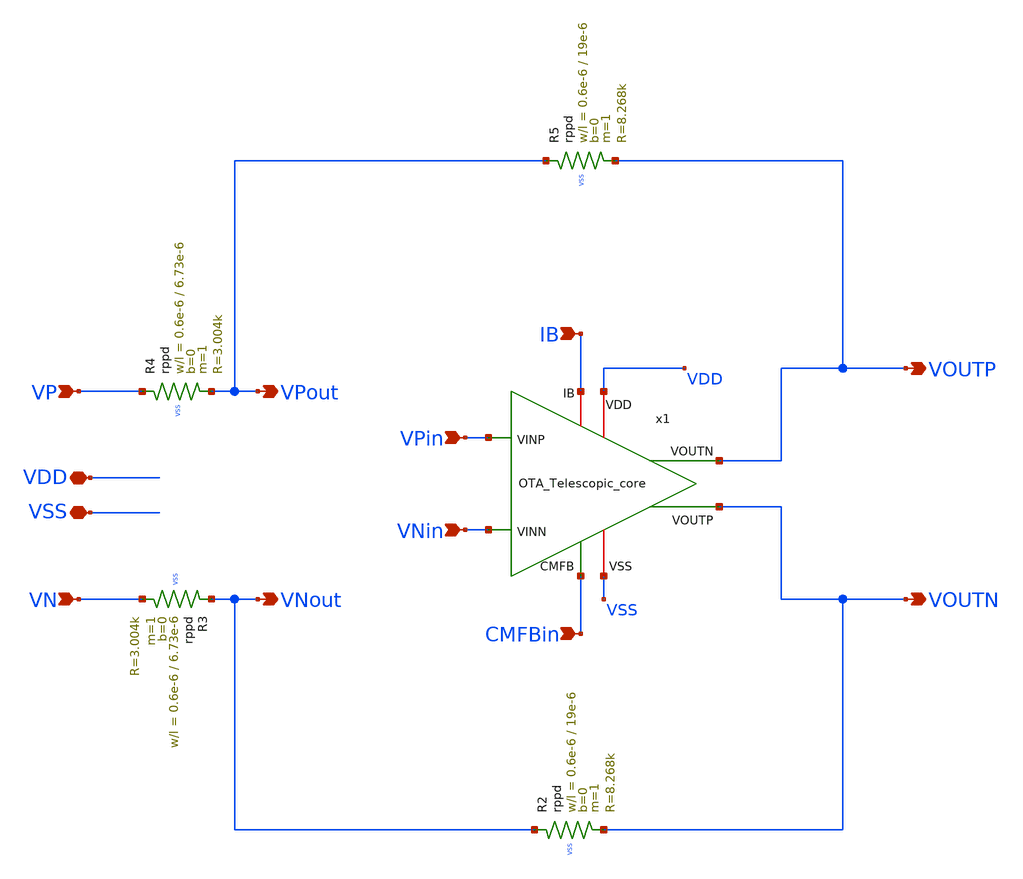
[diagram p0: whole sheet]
** sch_path: OTA_Telescopic_backup/OTA_Telescopic_NO_FLATTEN/Schematics_and_Symbols/OTA_Telescopic_FB.sch
**.subckt OTA_Telescopic_FB VP VN VOUTP VOUTN VPin VNin VPout VNout VDD VSS CMFBin IB
*.ipin VP
*.ipin VN
*.opin VOUTP
*.opin VOUTN
*.ipin VPin
*.ipin VNin
*.opin VPout
*.opin VNout
*.iopin VDD
*.iopin VSS
*.ipin CMFBin
*.ipin IB
x1 VDD CMFBin VOUTN VOUTP VPin VNin VSS IB OTA_Telescopic_core
XR3 VNout VN VSS rppd w=0.6e-6 l=6.73e-6 m=1 b=0 mm_ok=1
XR4 VP VPout VSS rppd w=0.6e-6 l=6.73e-6 m=1 b=0 mm_ok=1
XR5 VPout VOUTP VSS rppd w=0.6e-6 l=19e-6 m=1 b=0 mm_ok=1
XR2 VNout VOUTN VSS rppd w=0.6e-6 l=19e-6 m=1 b=0 mm_ok=1
**.ends

* expanding   symbol:  OTA_Telescopic_core.sym # of pins=8
** sym_path: OTA_Telescopic_core.sym
** sch_path: OTA_Telescopic_core.sch
.subckt OTA_Telescopic_core VDD CMFB VOUTP VOUTN VINP VINN VSS IB
*.iopin VDD
*.iopin VSS
*.ipin VINP
*.ipin VINN
*.opin VOUTN
*.opin VOUTP
*.ipin CMFB
*.iopin IB
V2 VB2 VSS 1.5
V3 VB3 VSS 0.7
V4 VB4 VSS 0.49409
V1 VB5 VSS 1.15
* noconn VB2
* noconn VB3
* noconn VB4
* noconn VB5
V5 VB VSS 0.90204
* noconn VB
XM15 VB55 VB55 VDD VDD sg13_lv_pmos w=1.4u l=0.35u ng=1 m=8 mm_ok=1
XM17 VB33 VB33 VDD VDD sg13_lv_pmos w=2.05u l=0.35u ng=1 m=1 mm_ok=1
XM18 VB22 VB33 VDD VDD sg13_lv_pmos w=2.05u l=0.35u ng=1 m=1 mm_ok=1
XM9 VOUTP Vo1 VDD VDD sg13_lv_pmos w=1.37u l=0.35u ng=1 m=250 mm_ok=1
XM7 Vx1 VB55 VDD VDD sg13_lv_pmos w=7u l=0.7u ng=1 m=30 mm_ok=1
XM5 Vo1 VB33 Vx1 VDD sg13_lv_pmos w=4.05u l=0.5u ng=1 m=30 mm_ok=1
XM8 Vx2 VB55 VDD VDD sg13_lv_pmos w=7u l=0.7u ng=1 m=30 mm_ok=1
XM6 Vo2 VB33 Vx2 VDD sg13_lv_pmos w=4.05u l=0.5u ng=1 m=30 mm_ok=1
XM10 VOUTN Vo2 VDD VDD sg13_lv_pmos w=1.37u l=0.35u ng=1 m=250 mm_ok=1
XM13 IB IB VSS VSS sg13_lv_nmos w=4.8u l=1.06u ng=1 m=1 mm_ok=1
XM14 VB55 IB VSS VSS sg13_lv_nmos w=4.8u l=1.06u ng=1 m=1 mm_ok=1
XM16 VB33 IB VSS VSS sg13_lv_nmos w=4.8u l=1.06u ng=1 m=1 mm_ok=1
XM19 VB22 VB22 VSS VSS sg13_lv_nmos w=0.5u l=0.8u ng=1 m=1 mm_ok=1
XM11 VOUTP IB VSS VSS sg13_lv_nmos w=4.8u l=1.06u ng=1 m=55 mm_ok=1
XM0 P CMFB VSS VSS sg13_lv_nmos w=30u l=0.20u ng=9 m=6 mm_ok=1
XM3 Vo1 VB22 Vy1 VSS sg13_lv_nmos w=1.9u l=0.16u ng=1 m=30 mm_ok=1
XM1 Vy1 VINP P VSS sg13_lv_nmos w=1.1u l=0.15u ng=1 m=30 mm_ok=1
XM4 Vo2 VB22 Vy2 VSS sg13_lv_nmos w=1.9u l=0.16u ng=1 m=30 mm_ok=1
XM2 Vy2 VINN P VSS sg13_lv_nmos w=1.1u l=0.15u ng=1 m=30 mm_ok=1
XM12 VOUTN IB VSS VSS sg13_lv_nmos w=4.8u l=1.06u ng=1 m=55 mm_ok=1
XR3 net1 VOUTP VSS rppd w=1.5e-6 l=0.55e-6 m=1 b=0 mm_ok=1
XR1 VOUTN net2 VSS rppd w=1.5e-6 l=0.55e-6 m=1 b=0 mm_ok=1
XC3 Vo2 net2 cap_cmim w=21.4e-6 l=21.4e-6 m=1 mm_ok=1
XC1 Vo1 net1 cap_cmim w=21.4e-6 l=21.4e-6 m=1 mm_ok=1
.ends

.end
